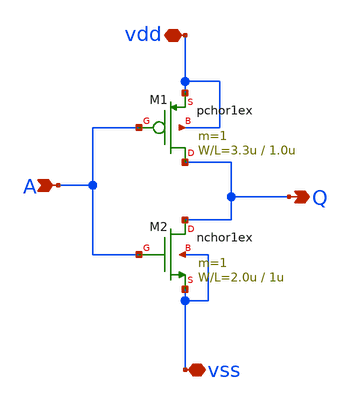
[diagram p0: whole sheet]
** sch_path: member_project/xian_DIY/xian_diy_1.sch
**.subckt xian_diy_1 vss vdd A Q
*.iopin vss
*.iopin vdd
*.ipin A
*.opin Q
M1 Q A vdd vdd pchor1ex L=1.0u W=3.3u m=1
M2 Q A vss vss nchor1ex L=1u W=2.0u m=1
**.ends
.end
